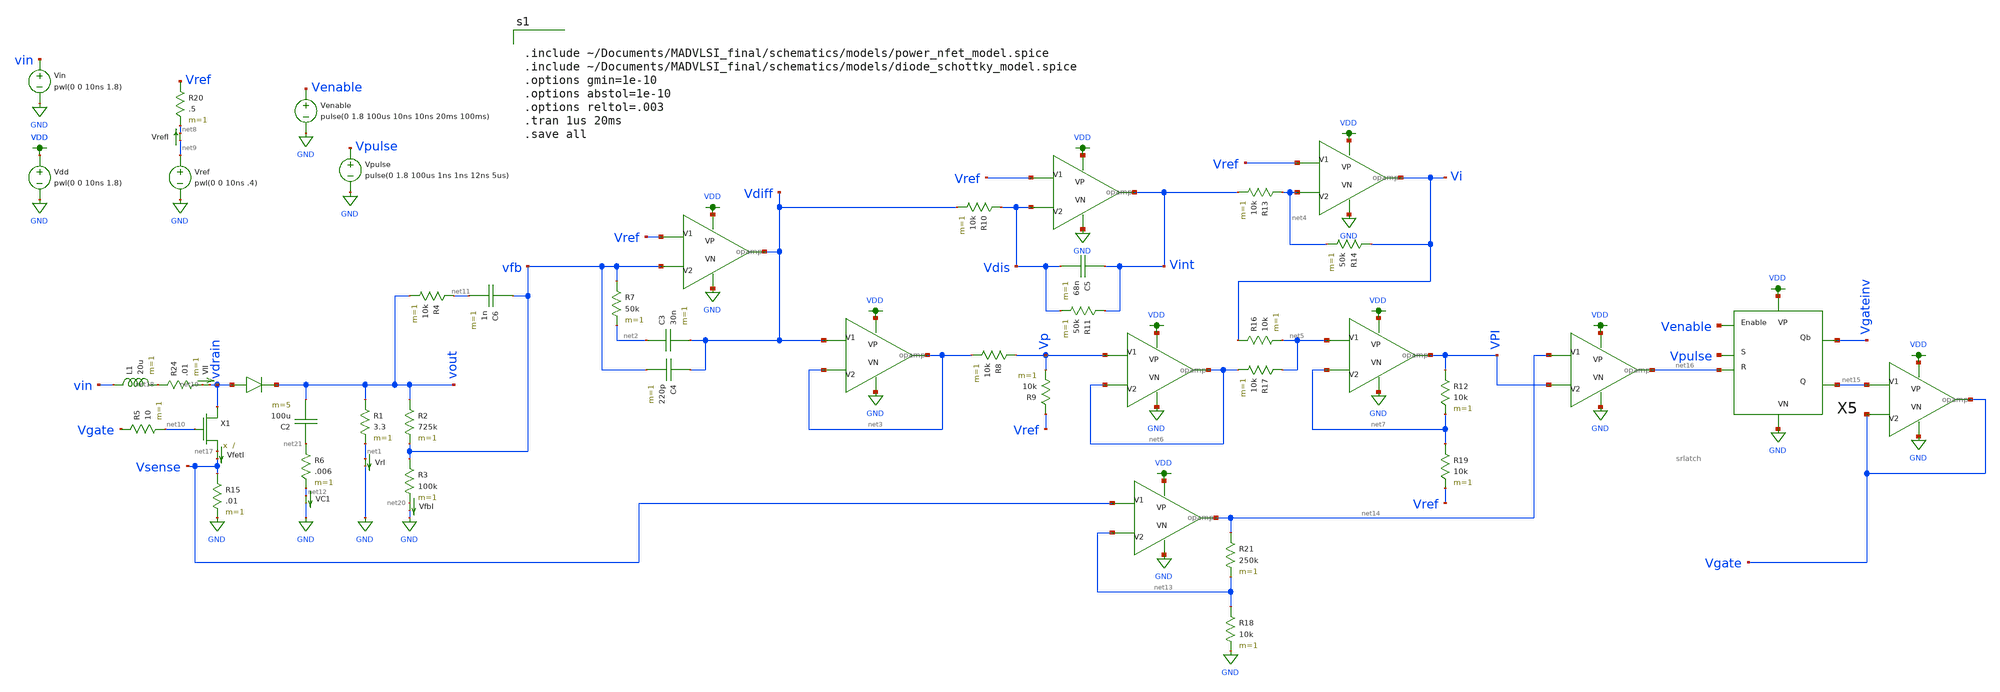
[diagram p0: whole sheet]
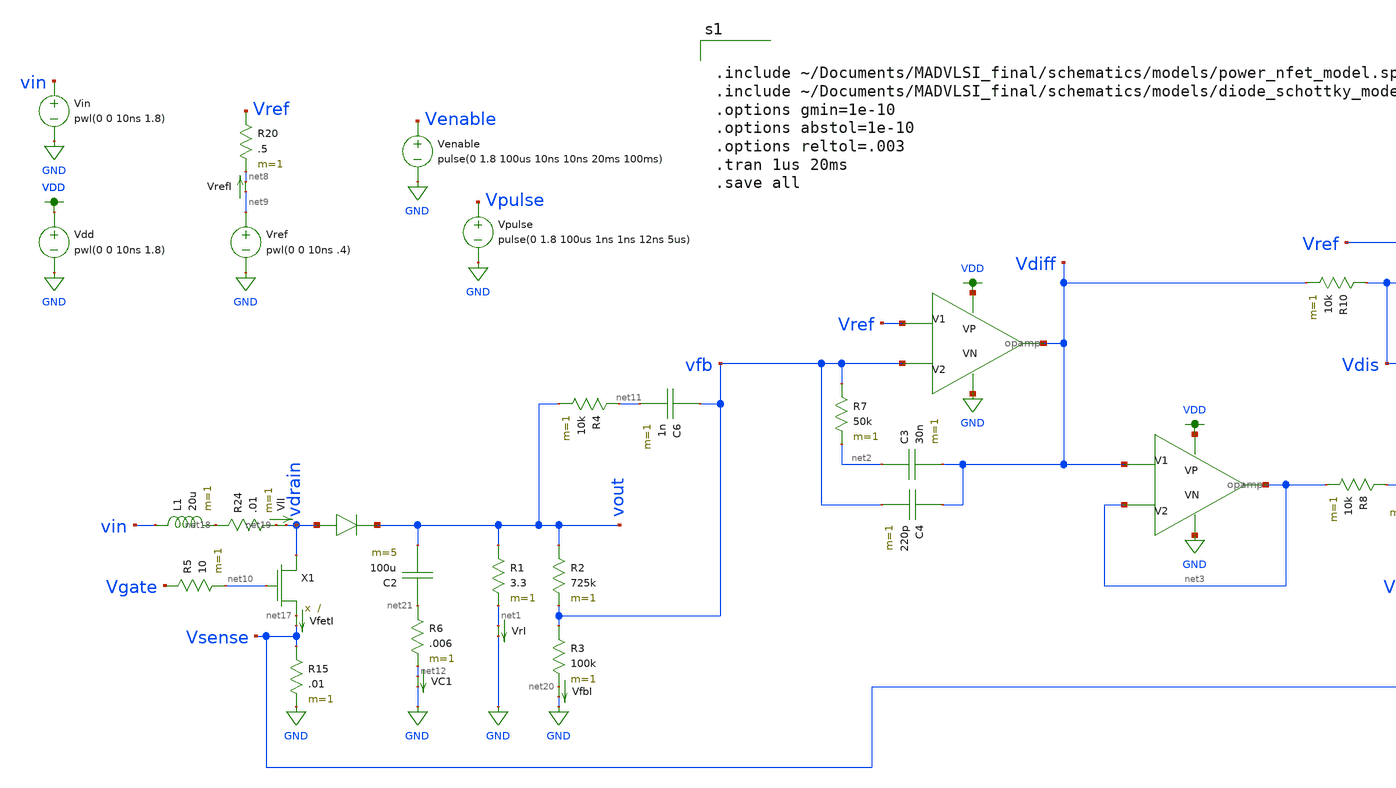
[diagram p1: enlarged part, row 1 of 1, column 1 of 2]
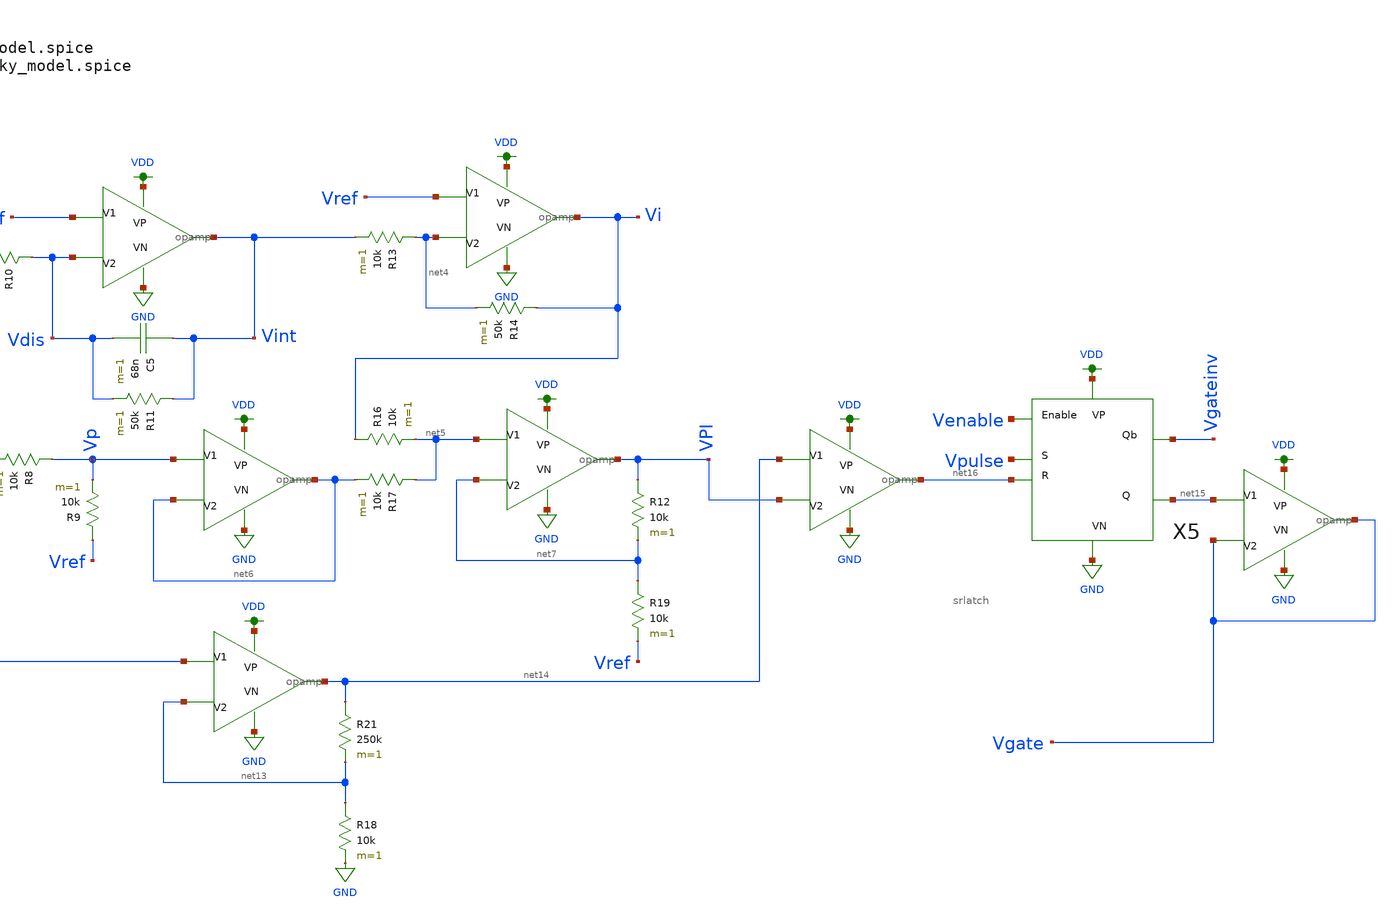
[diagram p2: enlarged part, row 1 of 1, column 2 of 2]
** sch_path: schematics/boost_CMC_tmp.sch
**.subckt boost_CMC_tmp
Vin vin GND pwl(0 0 10ns 1.8)
VfetI net17 Vsense 0
.save i(vfeti)
X1 vdrain net10 net17 power_nfet
L1 vin net18 20u m=1
D1 vdrain vout diode_schottky
R1 vout net1 3.3 m=1
VlI net19 vdrain 0
.save i(vli)
VrI net1 GND 0
.save i(vri)
R2 vout vfb 725k m=1
R3 vfb net20 100k m=1
Vdd VDD GND pwl(0 0 10ns 1.8)
Vref net9 GND pwl(0 0 10ns .4)
R7 vfb net2 50k m=1
X3 Vref vfb VDD GND Vdiff opamp
X4 Vdiff net3 VDD GND net3 opamp
R8 Vp net3 10k m=1
R9 Vref Vp 10k m=1
X6 Vref Vdis VDD GND Vint opamp
R10 Vdis Vdiff 10k m=1
C5 Vint Vdis 68n m=1
R11 Vint Vdis 50k m=1
X7 Vref net4 VDD GND Vi opamp
R13 net4 Vint 10k m=1
R14 Vi net4 50k m=1
X8 net5 net7 VDD GND VPI opamp
R16 Vi net5 10k m=1
R17 net5 net6 10k m=1
X9 Vp net6 VDD GND net6 opamp
R19 net7 Vref 10k m=1
X11 net14 VPI VDD GND net16 opamp
Vpulse Vpulse GND pulse(0 1.8 100us 1ns 1ns 12ns 5us)
VrefI net9 net8 0
.save i(vrefi)
R24 net18 net19 .01 m=1
VfbI net20 GND 0
.save i(vfbi)
R20 Vref net8 .5 m=1
R12 VPI net7 10k m=1
C3 net2 Vdiff 30n m=1
C4 Vdiff vfb 220p m=1
R4 net11 vout 10k m=1
C6 vfb net11 1n m=1
R5 Vgate net10 10 m=1
C2 net21 vout 100u m=5
R6 net21 net12 .006 m=1
VC1 net12 GND 0
.save i(vc1)
R15 Vsense GND .01 m=1
X2 Vsense net13 VDD GND net14 opamp
R18 net13 GND 10k m=1
R21 net14 net13 250k m=1
X5 Venable Vpulse net16 VDD GND Vgateinv net15 srlatch
X10 net15 Vgate VDD GND Vgate opamp
Venable Venable GND pulse(0 1.8 100us 10ns 10ns 20ms 100ms)
**** begin user architecture code


.include ~/Documents/MADVLSI_final/schematics/models/power_nfet_model.spice
.include ~/Documents/MADVLSI_final/schematics/models/diode_schottky_model.spice
.options gmin=1e-10
.options abstol=1e-10
.options reltol=.003
.tran 1us 20ms
.save all


.option wnflag=1
.lib ~/skywater/skywater-pdk/libraries/sky130_fd_pr_ngspice/latest/models/sky130.lib.spice tt

**** end user architecture code
**.ends

* expanding   symbol:  /home/madvlsi/Documents/MADVLSI_final/schematics/opamp.sym # of pins=5
** sym_path: schematics/opamp.sym
** sch_path: schematics/opamp.sch
.subckt opamp V1 V2 VP VN Vout
*.ipin V1
*.ipin V2
*.opin Vout
*.iopin VP
*.iopin VN
*.iopin VP
*.iopin VN
XM1 VN net7 net2 GND sky130_fd_pr__nfet_01v8 L=l W=w nf=1 ad='int((nf+1)/2) * W/nf * 0.29' as='int((nf+2)/2) * W/nf * 0.29'
+ pd='2*int((nf+1)/2) * (W/nf + 0.29)' ps='2*int((nf+2)/2) * (W/nf + 0.29)' nrd='0.29 / W' nrs='0.29 / W'
+ sa=0 sb=0 sd=0 mult=1 m=1
XM2 VP net3 net1 VDD sky130_fd_pr__pfet_01v8 L=l W=w nf=1 ad='int((nf+1)/2) * W/nf * 0.29' as='int((nf+2)/2) * W/nf * 0.29'
+ pd='2*int((nf+1)/2) * (W/nf + 0.29)' ps='2*int((nf+2)/2) * (W/nf + 0.29)' nrd='0.29 / W' nrs='0.29 / W'
+ sa=0 sb=0 sd=0 mult=1 m=1
XM3 net1 V1 Vd VDD sky130_fd_pr__pfet_01v8 L=l W=w nf=1 ad='int((nf+1)/2) * W/nf * 0.29' as='int((nf+2)/2) * W/nf * 0.29'
+ pd='2*int((nf+1)/2) * (W/nf + 0.29)' ps='2*int((nf+2)/2) * (W/nf + 0.29)' nrd='0.29 / W' nrs='0.29 / W'
+ sa=0 sb=0 sd=0 mult=1 m=1
XM4 Vc V2 net1 VDD sky130_fd_pr__pfet_01v8 L=l W=w nf=1 ad='int((nf+1)/2) * W/nf * 0.29' as='int((nf+2)/2) * W/nf * 0.29'
+ pd='2*int((nf+1)/2) * (W/nf + 0.29)' ps='2*int((nf+2)/2) * (W/nf + 0.29)' nrd='0.29 / W' nrs='0.29 / W'
+ sa=0 sb=0 sd=0 mult=1 m=1
XM5 Va V2 net2 GND sky130_fd_pr__nfet_01v8 L=l W=w nf=1 ad='int((nf+1)/2) * W/nf * 0.29' as='int((nf+2)/2) * W/nf * 0.29'
+ pd='2*int((nf+1)/2) * (W/nf + 0.29)' ps='2*int((nf+2)/2) * (W/nf + 0.29)' nrd='0.29 / W' nrs='0.29 / W'
+ sa=0 sb=0 sd=0 mult=1 m=1
XM6 net2 V1 Vb GND sky130_fd_pr__nfet_01v8 L=l W=w nf=1 ad='int((nf+1)/2) * W/nf * 0.29' as='int((nf+2)/2) * W/nf * 0.29'
+ pd='2*int((nf+1)/2) * (W/nf + 0.29)' ps='2*int((nf+2)/2) * (W/nf + 0.29)' nrd='0.29 / W' nrs='0.29 / W'
+ sa=0 sb=0 sd=0 mult=1 m=1
XM7 net3 net3 Va VDD sky130_fd_pr__pfet_01v8 L=l W=w nf=1 ad='int((nf+1)/2) * W/nf * 0.29' as='int((nf+2)/2) * W/nf * 0.29'
+ pd='2*int((nf+1)/2) * (W/nf + 0.29)' ps='2*int((nf+2)/2) * (W/nf + 0.29)' nrd='0.29 / W' nrs='0.29 / W'
+ sa=0 sb=0 sd=0 mult=1 m=1
XM8 net6 net6 Va VDD sky130_fd_pr__pfet_01v8 L=l W=w nf=1 ad='int((nf+1)/2) * W/nf * 0.29' as='int((nf+2)/2) * W/nf * 0.29'
+ pd='2*int((nf+1)/2) * (W/nf + 0.29)' ps='2*int((nf+2)/2) * (W/nf + 0.29)' nrd='0.29 / W' nrs='0.29 / W'
+ sa=0 sb=0 sd=0 mult=1 m=1
XM9 net5 net6 Vb VDD sky130_fd_pr__pfet_01v8 L=l W=w nf=1 ad='int((nf+1)/2) * W/nf * 0.29' as='int((nf+2)/2) * W/nf * 0.29'
+ pd='2*int((nf+1)/2) * (W/nf + 0.29)' ps='2*int((nf+2)/2) * (W/nf + 0.29)' nrd='0.29 / W' nrs='0.29 / W'
+ sa=0 sb=0 sd=0 mult=1 m=1
XM10 Va net3 VP VDD sky130_fd_pr__pfet_01v8 L=l W=w nf=1 ad='int((nf+1)/2) * W/nf * 0.29' as='int((nf+2)/2) * W/nf * 0.29'
+ pd='2*int((nf+1)/2) * (W/nf + 0.29)' ps='2*int((nf+2)/2) * (W/nf + 0.29)' nrd='0.29 / W' nrs='0.29 / W'
+ sa=0 sb=0 sd=0 mult=1 m=1
XM11 Vb net3 VP VDD sky130_fd_pr__pfet_01v8 L=l W=w nf=1 ad='int((nf+1)/2) * W/nf * 0.29' as='int((nf+2)/2) * W/nf * 0.29'
+ pd='2*int((nf+1)/2) * (W/nf + 0.29)' ps='2*int((nf+2)/2) * (W/nf + 0.29)' nrd='0.29 / W' nrs='0.29 / W'
+ sa=0 sb=0 sd=0 mult=1 m=1
XM12 net6 net6 Vc GND sky130_fd_pr__nfet_01v8 L=l W=w nf=1 ad='int((nf+1)/2) * W/nf * 0.29' as='int((nf+2)/2) * W/nf * 0.29'
+ pd='2*int((nf+1)/2) * (W/nf + 0.29)' ps='2*int((nf+2)/2) * (W/nf + 0.29)' nrd='0.29 / W' nrs='0.29 / W'
+ sa=0 sb=0 sd=0 mult=1 m=1
XM13 net5 net6 Vd GND sky130_fd_pr__nfet_01v8 L=l W=w nf=1 ad='int((nf+1)/2) * W/nf * 0.29' as='int((nf+2)/2) * W/nf * 0.29'
+ pd='2*int((nf+1)/2) * (W/nf + 0.29)' ps='2*int((nf+2)/2) * (W/nf + 0.29)' nrd='0.29 / W' nrs='0.29 / W'
+ sa=0 sb=0 sd=0 mult=1 m=1
XM14 Vc net7 VN GND sky130_fd_pr__nfet_01v8 L=l W=w nf=1 ad='int((nf+1)/2) * W/nf * 0.29' as='int((nf+2)/2) * W/nf * 0.29'
+ pd='2*int((nf+1)/2) * (W/nf + 0.29)' ps='2*int((nf+2)/2) * (W/nf + 0.29)' nrd='0.29 / W' nrs='0.29 / W'
+ sa=0 sb=0 sd=0 mult=1 m=1
XM15 Vd net7 VN GND sky130_fd_pr__nfet_01v8 L=l W=w nf=1 ad='int((nf+1)/2) * W/nf * 0.29' as='int((nf+2)/2) * W/nf * 0.29'
+ pd='2*int((nf+1)/2) * (W/nf + 0.29)' ps='2*int((nf+2)/2) * (W/nf + 0.29)' nrd='0.29 / W' nrs='0.29 / W'
+ sa=0 sb=0 sd=0 mult=1 m=1
XM16 net8 net7 net3 GND sky130_fd_pr__nfet_01v8 L=l W=w nf=1 ad='int((nf+1)/2) * W/nf * 0.29' as='int((nf+2)/2) * W/nf * 0.29'
+ pd='2*int((nf+1)/2) * (W/nf + 0.29)' ps='2*int((nf+2)/2) * (W/nf + 0.29)' nrd='0.29 / W' nrs='0.29 / W'
+ sa=0 sb=0 sd=0 mult=1 m=1
XM17 VN net7 net8 GND sky130_fd_pr__nfet_01v8 L=l W=w nf=1 ad='int((nf+1)/2) * W/nf * 0.29' as='int((nf+2)/2) * W/nf * 0.29'
+ pd='2*int((nf+1)/2) * (W/nf + 0.29)' ps='2*int((nf+2)/2) * (W/nf + 0.29)' nrd='0.29 / W' nrs='0.29 / W'
+ sa=0 sb=0 sd=0 mult=1 m=1
XM18 net8 net7 VP GND sky130_fd_pr__nfet_01v8 L=l W=w nf=1 ad='int((nf+1)/2) * W/nf * 0.29' as='int((nf+2)/2) * W/nf * 0.29'
+ pd='2*int((nf+1)/2) * (W/nf + 0.29)' ps='2*int((nf+2)/2) * (W/nf + 0.29)' nrd='0.29 / W' nrs='0.29 / W'
+ sa=0 sb=0 sd=0 mult=M m=M
XM19 net4 net3 net7 VDD sky130_fd_pr__pfet_01v8 L=l W=w nf=1 ad='int((nf+1)/2) * W/nf * 0.29' as='int((nf+2)/2) * W/nf * 0.29'
+ pd='2*int((nf+1)/2) * (W/nf + 0.29)' ps='2*int((nf+2)/2) * (W/nf + 0.29)' nrd='0.29 / W' nrs='0.29 / W'
+ sa=0 sb=0 sd=0 mult=1 m=1
XM20 VP net3 net4 VDD sky130_fd_pr__pfet_01v8 L=l W=w nf=1 ad='int((nf+1)/2) * W/nf * 0.29' as='int((nf+2)/2) * W/nf * 0.29'
+ pd='2*int((nf+1)/2) * (W/nf + 0.29)' ps='2*int((nf+2)/2) * (W/nf + 0.29)' nrd='0.29 / W' nrs='0.29 / W'
+ sa=0 sb=0 sd=0 mult=1 m=1
XM21 net4 net3 VN VDD sky130_fd_pr__pfet_01v8 L=l W=w nf=1 ad='int((nf+1)/2) * W/nf * 0.29' as='int((nf+2)/2) * W/nf * 0.29'
+ pd='2*int((nf+1)/2) * (W/nf + 0.29)' ps='2*int((nf+2)/2) * (W/nf + 0.29)' nrd='0.29 / W' nrs='0.29 / W'
+ sa=0 sb=0 sd=0 mult=M m=M
XM22 net7 net7 Vc GND sky130_fd_pr__nfet_01v8 L=l W=w nf=1 ad='int((nf+1)/2) * W/nf * 0.29' as='int((nf+2)/2) * W/nf * 0.29'
+ pd='2*int((nf+1)/2) * (W/nf + 0.29)' ps='2*int((nf+2)/2) * (W/nf + 0.29)' nrd='0.29 / W' nrs='0.29 / W'
+ sa=0 sb=0 sd=0 mult=1 m=1
**** begin user architecture code

.param M=3
.param w=3
.param l=0.6


**** end user architecture code
XM23 Vout net5 VN GND sky130_fd_pr__nfet_01v8 L=.15 W=6 nf=1 ad='int((nf+1)/2) * W/nf * 0.29' as='int((nf+2)/2) * W/nf * 0.29'
+ pd='2*int((nf+1)/2) * (W/nf + 0.29)' ps='2*int((nf+2)/2) * (W/nf + 0.29)' nrd='0.29 / W' nrs='0.29 / W'
+ sa=0 sb=0 sd=0 mult=1 m=1
XM24 Vout net5 VP VDD sky130_fd_pr__pfet_01v8 L=.15 W=12 nf=1 ad='int((nf+1)/2) * W/nf * 0.29' as='int((nf+2)/2) * W/nf * 0.29'
+ pd='2*int((nf+1)/2) * (W/nf + 0.29)' ps='2*int((nf+2)/2) * (W/nf + 0.29)' nrd='0.29 / W' nrs='0.29 / W'
+ sa=0 sb=0 sd=0 mult=1 m=1
C1 Vout net5 500f m=1
.ends


* expanding   symbol:  /home/madvlsi/Documents/MADVLSI_final/schematics/srlatch.sym # of pins=7
** sym_path: schematics/srlatch.sym
** sch_path: schematics/srlatch.sch
.subckt srlatch Enable S R VP VN Qb Q
*.ipin S
*.ipin R
*.iopin VP
*.iopin VN
*.opin Q
*.opin Qb
*.ipin Enable
X1 net1 Q VP VN Qb nor
X2 Qb net2 VP VN Q nor
X3 S Enable VP VN net1 and
X4 Enable R VP VN net2 and
.ends


* expanding   symbol:  /home/madvlsi/Documents/MADVLSI_final/schematics/nor.sym # of pins=5
** sym_path: schematics/nor.sym
** sch_path: schematics/nor.sch
.subckt nor A B VP VN Z
*.ipin A
*.ipin B
*.iopin VP
*.iopin VN
*.opin Z
**** begin user architecture code

.param l=.15
.param w=1

**** end user architecture code
XM1 Z A VN GND sky130_fd_pr__nfet_01v8 L=l W=w nf=1 ad='int((nf+1)/2) * W/nf * 0.29' as='int((nf+2)/2) * W/nf * 0.29'
+ pd='2*int((nf+1)/2) * (W/nf + 0.29)' ps='2*int((nf+2)/2) * (W/nf + 0.29)' nrd='0.29 / W' nrs='0.29 / W'
+ sa=0 sb=0 sd=0 mult=1 m=1
XM2 VN B Z GND sky130_fd_pr__nfet_01v8 L=l W=w nf=1 ad='int((nf+1)/2) * W/nf * 0.29' as='int((nf+2)/2) * W/nf * 0.29'
+ pd='2*int((nf+1)/2) * (W/nf + 0.29)' ps='2*int((nf+2)/2) * (W/nf + 0.29)' nrd='0.29 / W' nrs='0.29 / W'
+ sa=0 sb=0 sd=0 mult=1 m=1
XM3 Z A net1 VDD sky130_fd_pr__pfet_01v8 L=l W=w nf=1 ad='int((nf+1)/2) * W/nf * 0.29' as='int((nf+2)/2) * W/nf * 0.29'
+ pd='2*int((nf+1)/2) * (W/nf + 0.29)' ps='2*int((nf+2)/2) * (W/nf + 0.29)' nrd='0.29 / W' nrs='0.29 / W'
+ sa=0 sb=0 sd=0 mult=1 m=1
XM4 VP B net1 VDD sky130_fd_pr__pfet_01v8 L=l W=w nf=1 ad='int((nf+1)/2) * W/nf * 0.29' as='int((nf+2)/2) * W/nf * 0.29'
+ pd='2*int((nf+1)/2) * (W/nf + 0.29)' ps='2*int((nf+2)/2) * (W/nf + 0.29)' nrd='0.29 / W' nrs='0.29 / W'
+ sa=0 sb=0 sd=0 mult=1 m=1
.ends


* expanding   symbol:  /home/madvlsi/Documents/MADVLSI_final/schematics/and.sym # of pins=6
** sym_path: schematics/and.sym
** sch_path: schematics/and.sch
.subckt and A B VP VN Z
*.ipin A
*.ipin B
*.iopin VP
*.iopin VN
*.opin Z
X1 net1 VP VN Z inverter
X2 A B VP VN net1 nand
**** begin user architecture code

.param l=.15
.param w=1
.param mn=1
.param mp=1

**** end user architecture code
.ends


* expanding   symbol:  /home/madvlsi/Documents/final/xschem/inverter.sym # of pins=4
** sym_path: schematics/inverter.sym
** sch_path: schematics/inverter.sch
.subckt inverter A VP VN Z
*.ipin A
*.iopin VP
*.iopin VN
*.opin Z
XM1 Z A VN GND sky130_fd_pr__nfet_01v8 L=0.15 W=1 nf=1 ad='int((nf+1)/2) * W/nf * 0.29' as='int((nf+2)/2) * W/nf * 0.29'
+ pd='2*int((nf+1)/2) * (W/nf + 0.29)' ps='2*int((nf+2)/2) * (W/nf + 0.29)' nrd='0.29 / W' nrs='0.29 / W'
+ sa=0 sb=0 sd=0 mult=1 m=1
XM2 Z A VP VDD sky130_fd_pr__pfet_01v8 L=0.15 W=1 nf=1 ad='int((nf+1)/2) * W/nf * 0.29' as='int((nf+2)/2) * W/nf * 0.29'
+ pd='2*int((nf+1)/2) * (W/nf + 0.29)' ps='2*int((nf+2)/2) * (W/nf + 0.29)' nrd='0.29 / W' nrs='0.29 / W'
+ sa=0 sb=0 sd=0 mult=2 m=2
**** begin user architecture code

.param l=.15
.param w=1
.param mn=1
.param mp=1

**** end user architecture code
.ends


* expanding   symbol:  /home/madvlsi/Documents/final/xschem/nand.sym # of pins=6
** sym_path: schematics/nand.sym
** sch_path: schematics/nand.sch
.subckt nand A B VP VN Z
*.ipin A
*.iopin VP
*.iopin VN
*.opin Z
*.ipin B
XM1 Z A net1 GND sky130_fd_pr__nfet_01v8 L=0.15 W=1 nf=1 ad='int((nf+1)/2) * W/nf * 0.29' as='int((nf+2)/2) * W/nf * 0.29'
+ pd='2*int((nf+1)/2) * (W/nf + 0.29)' ps='2*int((nf+2)/2) * (W/nf + 0.29)' nrd='0.29 / W' nrs='0.29 / W'
+ sa=0 sb=0 sd=0 mult=1 m=1
XM2 VP B Z VDD sky130_fd_pr__pfet_01v8 L=0.15 W=1 nf=1 ad='int((nf+1)/2) * W/nf * 0.29' as='int((nf+2)/2) * W/nf * 0.29'
+ pd='2*int((nf+1)/2) * (W/nf + 0.29)' ps='2*int((nf+2)/2) * (W/nf + 0.29)' nrd='0.29 / W' nrs='0.29 / W'
+ sa=0 sb=0 sd=0 mult=2 m=2
XM3 VN B net1 GND sky130_fd_pr__nfet_01v8 L=0.15 W=1 nf=1 ad='int((nf+1)/2) * W/nf * 0.29' as='int((nf+2)/2) * W/nf * 0.29'
+ pd='2*int((nf+1)/2) * (W/nf + 0.29)' ps='2*int((nf+2)/2) * (W/nf + 0.29)' nrd='0.29 / W' nrs='0.29 / W'
+ sa=0 sb=0 sd=0 mult=1 m=1
XM4 Z A VP VDD sky130_fd_pr__pfet_01v8 L=0.15 W=1 nf=1 ad='int((nf+1)/2) * W/nf * 0.29' as='int((nf+2)/2) * W/nf * 0.29'
+ pd='2*int((nf+1)/2) * (W/nf + 0.29)' ps='2*int((nf+2)/2) * (W/nf + 0.29)' nrd='0.29 / W' nrs='0.29 / W'
+ sa=0 sb=0 sd=0 mult=2 m=2
.ends

.GLOBAL GND
.GLOBAL VDD
.end
